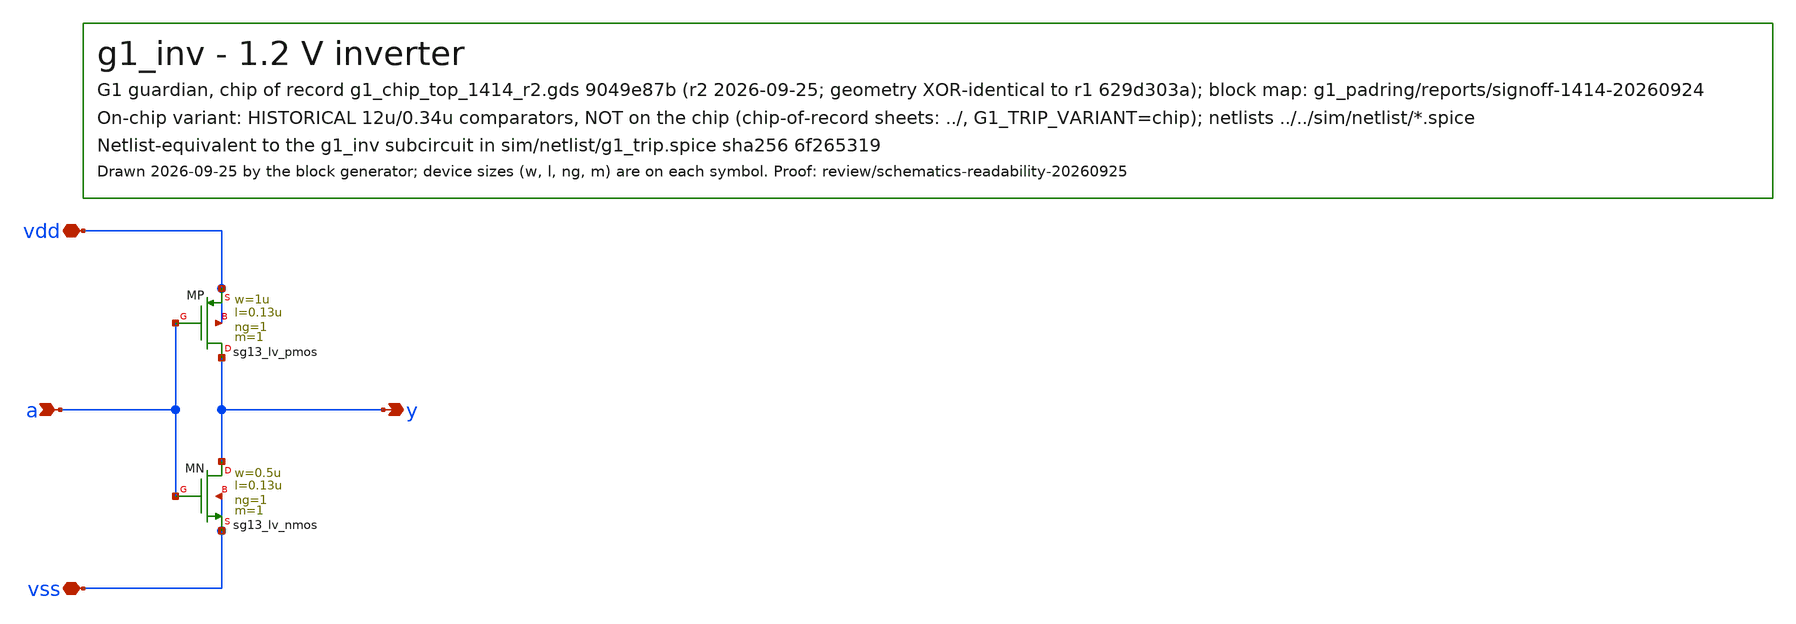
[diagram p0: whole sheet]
** sch_path: designs/g1-guardian/blocks/g1_trip/schematic/historical_12u034/g1_inv.sch
**.subckt g1_inv a y vdd vss
*.ipin a
*.opin y
*.iopin vdd
*.iopin vss
XMP y a vdd vdd sg13_lv_pmos w=1u l=0.13u ng=1 m=1 mm_ok=1
XMN y a vss vss sg13_lv_nmos w=0.5u l=0.13u ng=1 m=1 mm_ok=1
**.ends
.end
